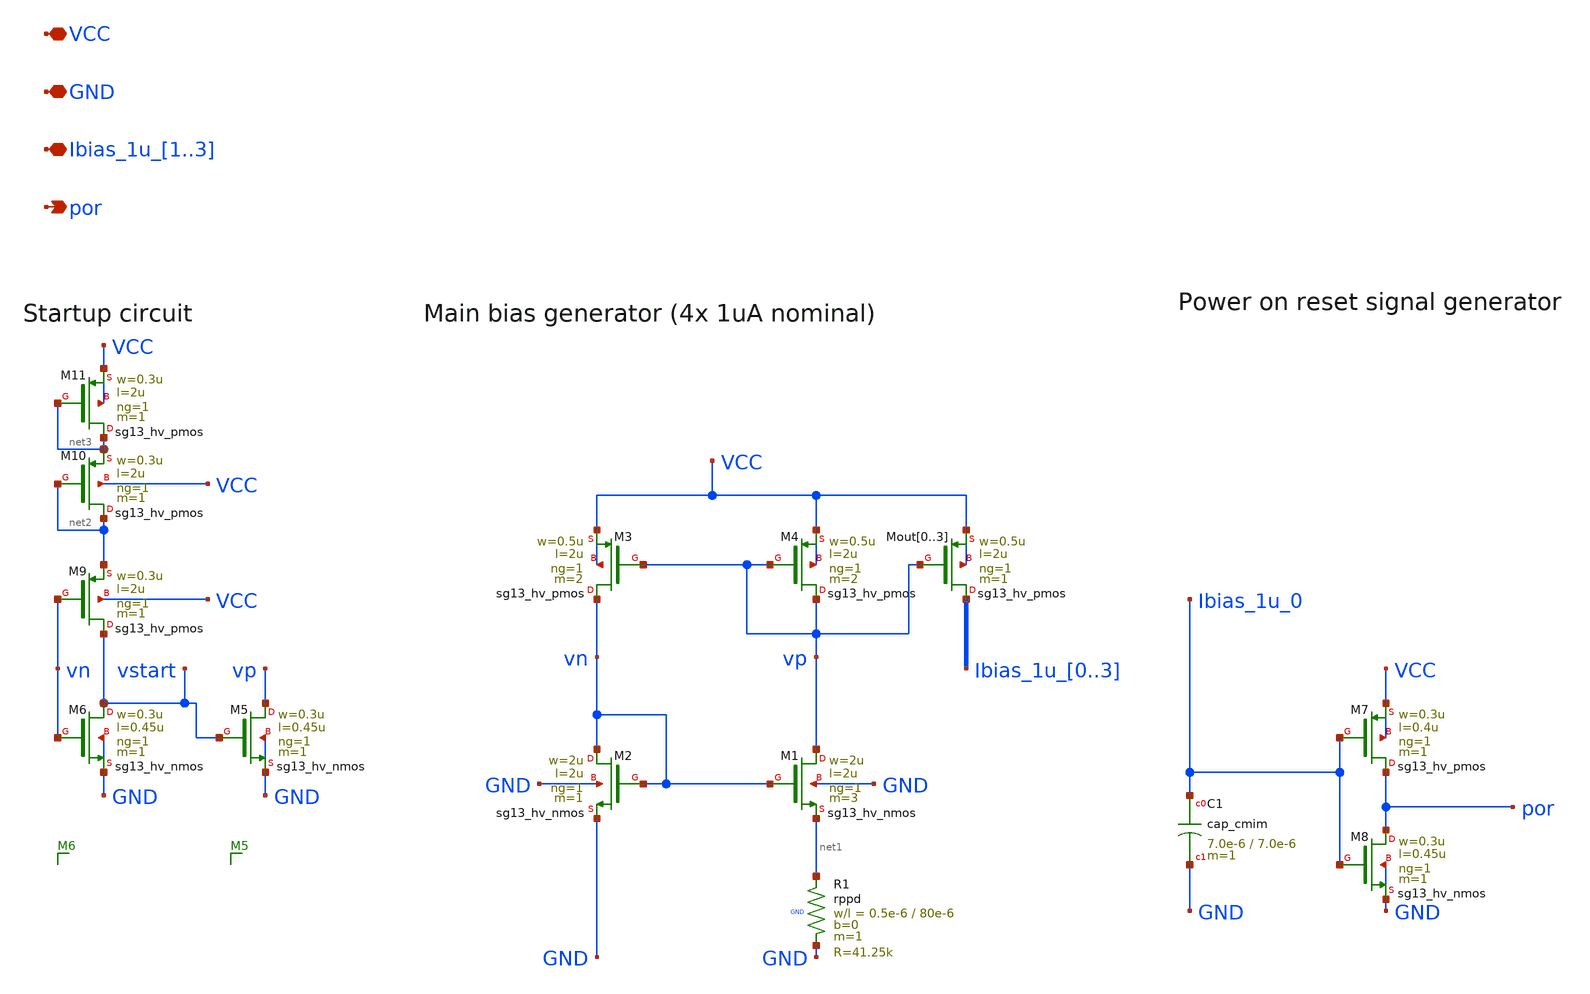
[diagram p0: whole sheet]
** sch_path: FLDO/design_data/xschem/biasgen.sch
**.subckt biasgen VCC GND Ibias_1u_1,Ibias_1u_2,Ibias_1u_3 por
*.iopin VCC
*.iopin GND
*.iopin Ibias_1u_1,Ibias_1u_2,Ibias_1u_3
*.opin por
XM1 vp vn net1 GND sg13_hv_nmos w=2u l=2u ng=1 m=3 mm_ok=1
XM2 vn vn GND GND sg13_hv_nmos w=2u l=2u ng=1 m=1 mm_ok=1
XM3 vn vp VCC VCC sg13_hv_pmos w=0.5u l=2u ng=1 m=2 mm_ok=1
XM4 vp vp VCC VCC sg13_hv_pmos w=0.5u l=2u ng=1 m=2 mm_ok=1
XMout0 Ibias_1u_0 vp VCC VCC sg13_hv_pmos w=0.5u l=2u ng=1 m=1 mm_ok=1
XMout1 Ibias_1u_1 vp VCC VCC sg13_hv_pmos w=0.5u l=2u ng=1 m=1 mm_ok=1
XMout2 Ibias_1u_2 vp VCC VCC sg13_hv_pmos w=0.5u l=2u ng=1 m=1 mm_ok=1
XMout3 Ibias_1u_3 vp VCC VCC sg13_hv_pmos w=0.5u l=2u ng=1 m=1 mm_ok=1
XC1 Ibias_1u_0 GND cap_cmim w=7.0e-6 l=7.0e-6 m=1
XM7 por Ibias_1u_0 VCC VCC sg13_hv_pmos w=0.3u l=0.4u ng=1 m=1 mm_ok=1
XM8 por Ibias_1u_0 GND GND sg13_hv_nmos w=0.3u l=0.45u ng=1 m=1 mm_ok=1
XR1 net1 GND GND rppd w=0.5e-6 l=80e-6 m=1 b=0 mm_ok=1
XM5 vp vstart GND GND sg13_hv_nmos w=0.3u l=0.45u ng=1 m=1 mm_ok=1
XM6 vstart vn GND GND sg13_hv_nmos w=0.3u l=0.45u ng=1 m=1 mm_ok=1
XM9 vstart vn net2 VCC sg13_hv_pmos w=0.3u l=2u ng=1 m=1 mm_ok=1
XM10 net2 net2 net3 VCC sg13_hv_pmos w=0.3u l=2u ng=1 m=1 mm_ok=1
XM11 net3 net3 VCC VCC sg13_hv_pmos w=0.3u l=2u ng=1 m=1 mm_ok=1
**.ends
.end
